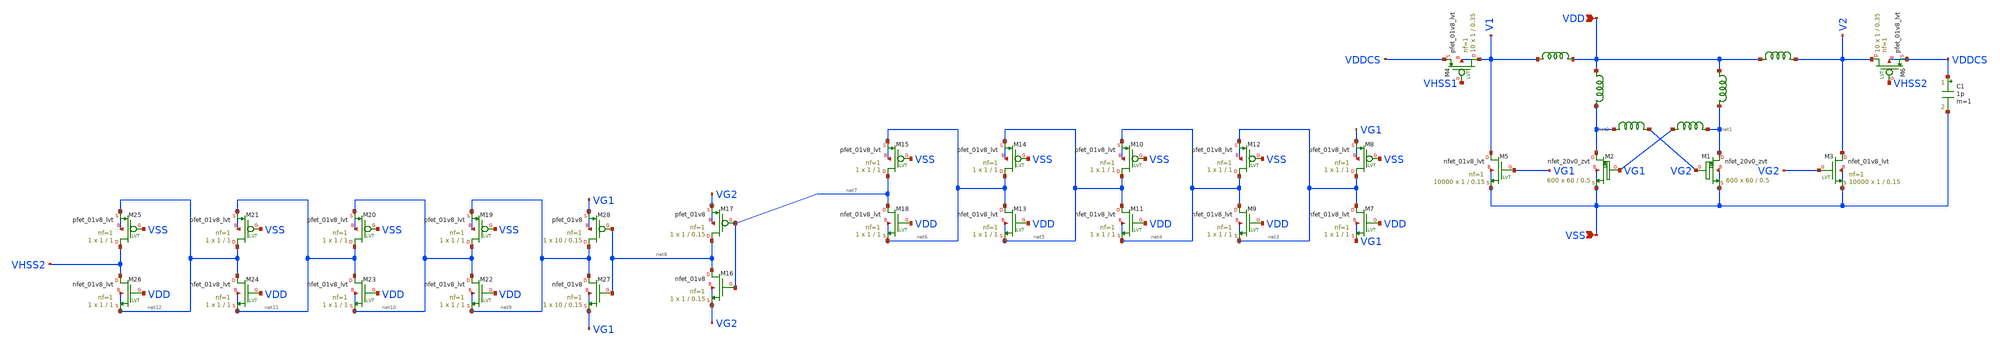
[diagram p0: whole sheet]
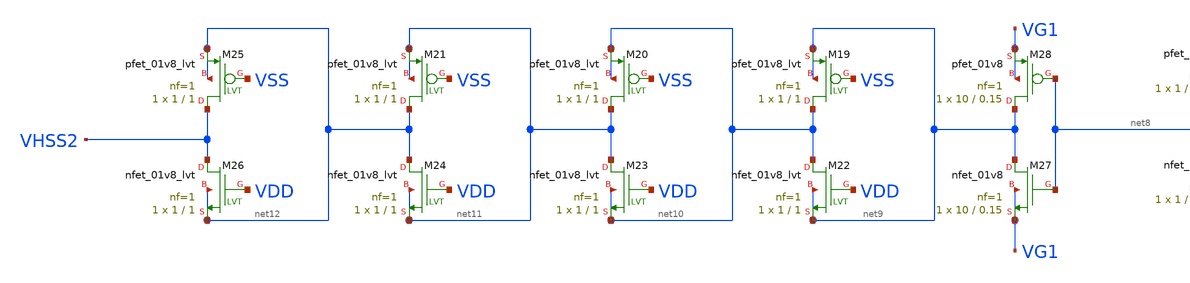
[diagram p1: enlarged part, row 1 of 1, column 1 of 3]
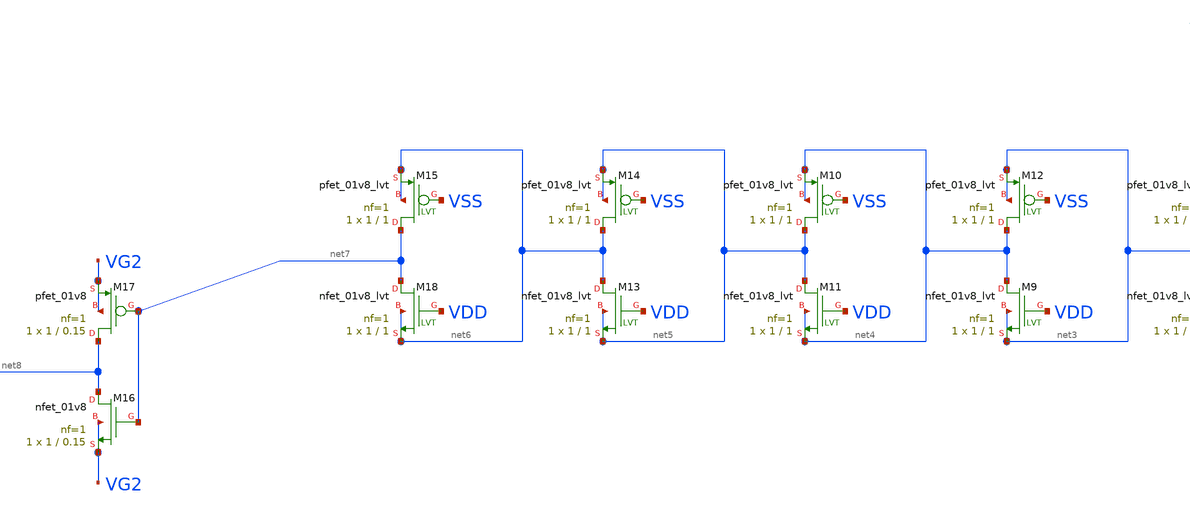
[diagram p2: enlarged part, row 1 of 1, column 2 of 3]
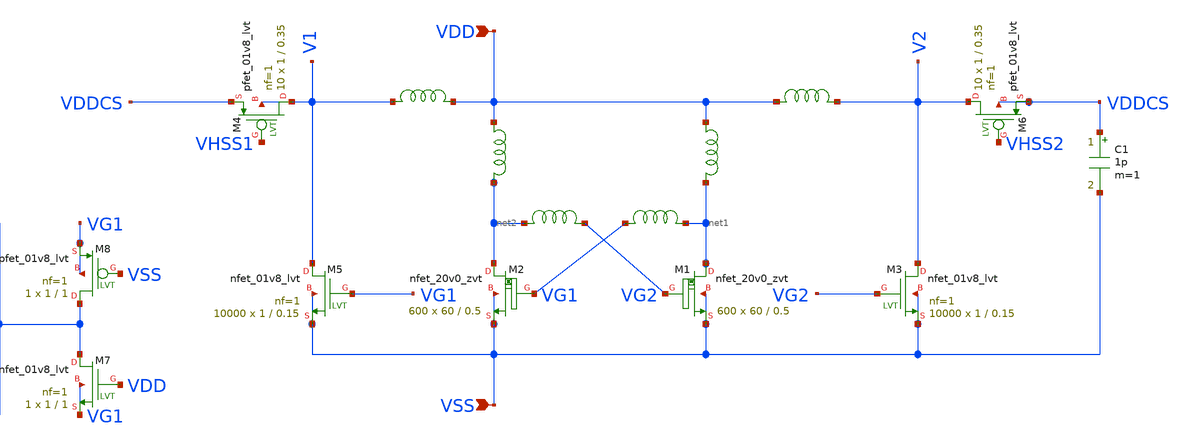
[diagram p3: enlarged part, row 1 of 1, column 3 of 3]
** sch_path: design/LELO_SVOD_SKY130A/LELO_EXSCtwostage.sch
**.subckt LELO_EXSCtwostage VSS VDD
*.ipin VSS
*.ipin VDD
x3 VDD net1 1812PS-102_imp
x4 VDD net2 1812PS-102_imp
XM1 net1 VG2 VSS VSS sky130_fd_pr__nfet_20v0_zvt W=60 L=0.5 m=600
XM2 net2 VG1 VSS VSS sky130_fd_pr__nfet_20v0_zvt W=60 L=0.5 m=600
x1 net2 VG2 1812PS-104_imp
x2 VG1 net1 1812PS-104_imp
C1 VDDCS VSS 1p m=1
x5 VDD V1 1812PS-334_imp
x6 VDD V2 1812PS-334_imp
XM3 V2 VG2 VSS VSS sky130_fd_pr__nfet_01v8_lvt L=0.15 W=1 nf=1 ad='int((1 + 1)/2) * 1 / 1 * 0.29' as='int((1 + 2)/2) * 1 / 1 * 0.29'
+ pd='2*int((1 + 1)/2) * (1 / 1 + 0.29)' ps='2*int((1 + 2)/2) * (1 / 1 + 0.29)' nrd='0.29 / 1 ' nrs='0.29 / 1 '
+ sa=0 sb=0 sd=0 mult=10000 m=10000
XM5 V1 VG1 VSS VSS sky130_fd_pr__nfet_01v8_lvt L=0.15 W=1 nf=1 ad='int((1 + 1)/2) * 1 / 1 * 0.29' as='int((1 + 2)/2) * 1 / 1 * 0.29'
+ pd='2*int((1 + 1)/2) * (1 / 1 + 0.29)' ps='2*int((1 + 2)/2) * (1 / 1 + 0.29)' nrd='0.29 / 1 ' nrs='0.29 / 1 '
+ sa=0 sb=0 sd=0 mult=10000 m=10000
XM6 V2 VHSS2 VDDCS VDDCS sky130_fd_pr__pfet_01v8_lvt L=0.35 W=1 nf=1 ad='int((1 + 1)/2) * 1 / 1 * 0.29'
+ as='int((1 + 2)/2) * 1 / 1 * 0.29' pd='2*int((1 + 1)/2) * (1 / 1 + 0.29)' ps='2*int((1 + 2)/2) * (1 / 1 + 0.29)'
+ nrd='0.29 / 1 ' nrs='0.29 / 1 ' sa=0 sb=0 sd=0 mult=10 m=10
XM4 V1 VHSS1 VDDCS V1 sky130_fd_pr__pfet_01v8_lvt L=0.35 W=1 nf=1 ad='int((1 + 1)/2) * 1 / 1 * 0.29'
+ as='int((1 + 2)/2) * 1 / 1 * 0.29' pd='2*int((1 + 1)/2) * (1 / 1 + 0.29)' ps='2*int((1 + 2)/2) * (1 / 1 + 0.29)'
+ nrd='0.29 / 1 ' nrs='0.29 / 1 ' sa=0 sb=0 sd=0 mult=10 m=10
XM8 net3 VSS VG1 VG1 sky130_fd_pr__pfet_01v8_lvt L=1 W=1 nf=1 ad='int((1 + 1)/2) * 1 / 1 * 0.29' as='int((1 + 2)/2) * 1 / 1 * 0.29'
+ pd='2*int((1 + 1)/2) * (1 / 1 + 0.29)' ps='2*int((1 + 2)/2) * (1 / 1 + 0.29)' nrd='0.29 / 1 ' nrs='0.29 / 1 '
+ sa=0 sb=0 sd=0 mult=1 m=1
XM12 net4 VSS net3 net3 sky130_fd_pr__pfet_01v8_lvt L=1 W=1 nf=1 ad='int((1 + 1)/2) * 1 / 1 * 0.29' as='int((1 + 2)/2) * 1 / 1 * 0.29'
+ pd='2*int((1 + 1)/2) * (1 / 1 + 0.29)' ps='2*int((1 + 2)/2) * (1 / 1 + 0.29)' nrd='0.29 / 1 ' nrs='0.29 / 1 '
+ sa=0 sb=0 sd=0 mult=1 m=1
XM10 net5 VSS net4 net4 sky130_fd_pr__pfet_01v8_lvt L=1 W=1 nf=1 ad='int((1 + 1)/2) * 1 / 1 * 0.29' as='int((1 + 2)/2) * 1 / 1 * 0.29'
+ pd='2*int((1 + 1)/2) * (1 / 1 + 0.29)' ps='2*int((1 + 2)/2) * (1 / 1 + 0.29)' nrd='0.29 / 1 ' nrs='0.29 / 1 '
+ sa=0 sb=0 sd=0 mult=1 m=1
XM14 net6 VSS net5 net5 sky130_fd_pr__pfet_01v8_lvt L=1 W=1 nf=1 ad='int((1 + 1)/2) * 1 / 1 * 0.29' as='int((1 + 2)/2) * 1 / 1 * 0.29'
+ pd='2*int((1 + 1)/2) * (1 / 1 + 0.29)' ps='2*int((1 + 2)/2) * (1 / 1 + 0.29)' nrd='0.29 / 1 ' nrs='0.29 / 1 '
+ sa=0 sb=0 sd=0 mult=1 m=1
XM7 net3 VDD VG1 VG1 sky130_fd_pr__nfet_01v8_lvt L=1 W=1 nf=1 ad='int((1 + 1)/2) * 1 / 1 * 0.29' as='int((1 + 2)/2) * 1 / 1 * 0.29'
+ pd='2*int((1 + 1)/2) * (1 / 1 + 0.29)' ps='2*int((1 + 2)/2) * (1 / 1 + 0.29)' nrd='0.29 / 1 ' nrs='0.29 / 1 '
+ sa=0 sb=0 sd=0 mult=1 m=1
XM9 net4 VDD net3 net3 sky130_fd_pr__nfet_01v8_lvt L=1 W=1 nf=1 ad='int((1 + 1)/2) * 1 / 1 * 0.29' as='int((1 + 2)/2) * 1 / 1 * 0.29'
+ pd='2*int((1 + 1)/2) * (1 / 1 + 0.29)' ps='2*int((1 + 2)/2) * (1 / 1 + 0.29)' nrd='0.29 / 1 ' nrs='0.29 / 1 '
+ sa=0 sb=0 sd=0 mult=1 m=1
XM11 net5 VDD net4 net4 sky130_fd_pr__nfet_01v8_lvt L=1 W=1 nf=1 ad='int((1 + 1)/2) * 1 / 1 * 0.29' as='int((1 + 2)/2) * 1 / 1 * 0.29'
+ pd='2*int((1 + 1)/2) * (1 / 1 + 0.29)' ps='2*int((1 + 2)/2) * (1 / 1 + 0.29)' nrd='0.29 / 1 ' nrs='0.29 / 1 '
+ sa=0 sb=0 sd=0 mult=1 m=1
XM13 net6 VDD net5 net5 sky130_fd_pr__nfet_01v8_lvt L=1 W=1 nf=1 ad='int((1 + 1)/2) * 1 / 1 * 0.29' as='int((1 + 2)/2) * 1 / 1 * 0.29'
+ pd='2*int((1 + 1)/2) * (1 / 1 + 0.29)' ps='2*int((1 + 2)/2) * (1 / 1 + 0.29)' nrd='0.29 / 1 ' nrs='0.29 / 1 '
+ sa=0 sb=0 sd=0 mult=1 m=1
XM15 net7 VSS net6 net6 sky130_fd_pr__pfet_01v8_lvt L=1 W=1 nf=1 ad='int((1 + 1)/2) * 1 / 1 * 0.29' as='int((1 + 2)/2) * 1 / 1 * 0.29'
+ pd='2*int((1 + 1)/2) * (1 / 1 + 0.29)' ps='2*int((1 + 2)/2) * (1 / 1 + 0.29)' nrd='0.29 / 1 ' nrs='0.29 / 1 '
+ sa=0 sb=0 sd=0 mult=1 m=1
XM18 net7 VDD net6 net6 sky130_fd_pr__nfet_01v8_lvt L=1 W=1 nf=1 ad='int((1 + 1)/2) * 1 / 1 * 0.29' as='int((1 + 2)/2) * 1 / 1 * 0.29'
+ pd='2*int((1 + 1)/2) * (1 / 1 + 0.29)' ps='2*int((1 + 2)/2) * (1 / 1 + 0.29)' nrd='0.29 / 1 ' nrs='0.29 / 1 '
+ sa=0 sb=0 sd=0 mult=1 m=1
XM16 net8 net7 VG2 VG2 sky130_fd_pr__nfet_01v8 L=0.15 W=1 nf=1 ad='int((1 + 1)/2) * 1 / 1 * 0.29' as='int((1 + 2)/2) * 1 / 1 * 0.29'
+ pd='2*int((1 + 1)/2) * (1 / 1 + 0.29)' ps='2*int((1 + 2)/2) * (1 / 1 + 0.29)' nrd='0.29 / 1 ' nrs='0.29 / 1 '
+ sa=0 sb=0 sd=0 mult=1 m=1
XM17 net8 net7 VG2 VG2 sky130_fd_pr__pfet_01v8 L=0.15 W=1 nf=1 ad='int((1 + 1)/2) * 1 / 1 * 0.29' as='int((1 + 2)/2) * 1 / 1 * 0.29'
+ pd='2*int((1 + 1)/2) * (1 / 1 + 0.29)' ps='2*int((1 + 2)/2) * (1 / 1 + 0.29)' nrd='0.29 / 1 ' nrs='0.29 / 1 '
+ sa=0 sb=0 sd=0 mult=1 m=1
XM27 net9 net8 VG1 VG1 sky130_fd_pr__nfet_01v8 L=0.15 W=10 nf=1 ad='int((1 + 1)/2) * 10 / 1 * 0.29' as='int((1 + 2)/2) * 10 / 1 * 0.29'
+ pd='2*int((1 + 1)/2) * (10 / 1 + 0.29)' ps='2*int((1 + 2)/2) * (10 / 1 + 0.29)' nrd='0.29 / 10 ' nrs='0.29 / 10 '
+ sa=0 sb=0 sd=0 mult=1 m=1
XM28 net9 net8 VG1 VG1 sky130_fd_pr__pfet_01v8 L=0.15 W=10 nf=1 ad='int((1 + 1)/2) * 10 / 1 * 0.29' as='int((1 + 2)/2) * 10 / 1 * 0.29'
+ pd='2*int((1 + 1)/2) * (10 / 1 + 0.29)' ps='2*int((1 + 2)/2) * (10 / 1 + 0.29)' nrd='0.29 / 10 ' nrs='0.29 / 10 '
+ sa=0 sb=0 sd=0 mult=1 m=1
XM19 net10 VSS net9 net9 sky130_fd_pr__pfet_01v8_lvt L=1 W=1 nf=1 ad='int((1 + 1)/2) * 1 / 1 * 0.29'
+ as='int((1 + 2)/2) * 1 / 1 * 0.29' pd='2*int((1 + 1)/2) * (1 / 1 + 0.29)' ps='2*int((1 + 2)/2) * (1 / 1 + 0.29)'
+ nrd='0.29 / 1 ' nrs='0.29 / 1 ' sa=0 sb=0 sd=0 mult=1 m=1
XM20 net11 VSS net10 net10 sky130_fd_pr__pfet_01v8_lvt L=1 W=1 nf=1 ad='int((1 + 1)/2) * 1 / 1 * 0.29'
+ as='int((1 + 2)/2) * 1 / 1 * 0.29' pd='2*int((1 + 1)/2) * (1 / 1 + 0.29)' ps='2*int((1 + 2)/2) * (1 / 1 + 0.29)'
+ nrd='0.29 / 1 ' nrs='0.29 / 1 ' sa=0 sb=0 sd=0 mult=1 m=1
XM21 net12 VSS net11 net11 sky130_fd_pr__pfet_01v8_lvt L=1 W=1 nf=1 ad='int((1 + 1)/2) * 1 / 1 * 0.29'
+ as='int((1 + 2)/2) * 1 / 1 * 0.29' pd='2*int((1 + 1)/2) * (1 / 1 + 0.29)' ps='2*int((1 + 2)/2) * (1 / 1 + 0.29)'
+ nrd='0.29 / 1 ' nrs='0.29 / 1 ' sa=0 sb=0 sd=0 mult=1 m=1
XM22 net10 VDD net9 net9 sky130_fd_pr__nfet_01v8_lvt L=1 W=1 nf=1 ad='int((1 + 1)/2) * 1 / 1 * 0.29'
+ as='int((1 + 2)/2) * 1 / 1 * 0.29' pd='2*int((1 + 1)/2) * (1 / 1 + 0.29)' ps='2*int((1 + 2)/2) * (1 / 1 + 0.29)'
+ nrd='0.29 / 1 ' nrs='0.29 / 1 ' sa=0 sb=0 sd=0 mult=1 m=1
XM23 net11 VDD net10 net10 sky130_fd_pr__nfet_01v8_lvt L=1 W=1 nf=1 ad='int((1 + 1)/2) * 1 / 1 * 0.29'
+ as='int((1 + 2)/2) * 1 / 1 * 0.29' pd='2*int((1 + 1)/2) * (1 / 1 + 0.29)' ps='2*int((1 + 2)/2) * (1 / 1 + 0.29)'
+ nrd='0.29 / 1 ' nrs='0.29 / 1 ' sa=0 sb=0 sd=0 mult=1 m=1
XM24 net12 VDD net11 net11 sky130_fd_pr__nfet_01v8_lvt L=1 W=1 nf=1 ad='int((1 + 1)/2) * 1 / 1 * 0.29'
+ as='int((1 + 2)/2) * 1 / 1 * 0.29' pd='2*int((1 + 1)/2) * (1 / 1 + 0.29)' ps='2*int((1 + 2)/2) * (1 / 1 + 0.29)'
+ nrd='0.29 / 1 ' nrs='0.29 / 1 ' sa=0 sb=0 sd=0 mult=1 m=1
XM25 VHSS2 VSS net12 net12 sky130_fd_pr__pfet_01v8_lvt L=1 W=1 nf=1 ad='int((1 + 1)/2) * 1 / 1 * 0.29'
+ as='int((1 + 2)/2) * 1 / 1 * 0.29' pd='2*int((1 + 1)/2) * (1 / 1 + 0.29)' ps='2*int((1 + 2)/2) * (1 / 1 + 0.29)'
+ nrd='0.29 / 1 ' nrs='0.29 / 1 ' sa=0 sb=0 sd=0 mult=1 m=1
XM26 VHSS2 VDD net12 net12 sky130_fd_pr__nfet_01v8_lvt L=1 W=1 nf=1 ad='int((1 + 1)/2) * 1 / 1 * 0.29'
+ as='int((1 + 2)/2) * 1 / 1 * 0.29' pd='2*int((1 + 1)/2) * (1 / 1 + 0.29)' ps='2*int((1 + 2)/2) * (1 / 1 + 0.29)'
+ nrd='0.29 / 1 ' nrs='0.29 / 1 ' sa=0 sb=0 sd=0 mult=1 m=1
**.ends

* expanding   symbol:  LELO_SVOD_SKY130A/1812PS-102_imp.sym # of pins=2
** sym_path: design/LELO_SVOD_SKY130A/1812PS-102_imp.sym

.subckt 1812PS-102_imp port1 port2
X1 port1 port2 Model1D R1=60 R2=0.054 C= 0.15p K1=0.000001 K2=0.064 K3= 1u K4=1E-06 K5=0.000001 L=0
+ Is=0 a=0 L_Z0=0 L_EL=0 L_F0=0E6 PkZ=1282.46492
.ends 1812PS-102_imp

* expanding   symbol:  LELO_SVOD_SKY130A/1812PS-104_imp.sym # of pins=2
** sym_path: design/LELO_SVOD_SKY130A/1812PS-104_imp.sym

.subckt 1812PS-104_imp port1 port2
X1 port1 port2 Model1D R1=40 R2=1.3 C= 1.6p K1=0.000001 K2=13.98 K3= 100u K4=0.000001 K5=0.000001
+ L=0 Is=0 a=0 L_Z0=0 L_EL=0 L_F0=0E6 PkZ=48065.0165
.ends 1812PS-104_imp

* expanding   symbol:  LELO_SVOD_SKY130A/1812PS-334_imp.sym # of pins=2
** sym_path: design/LELO_SVOD_SKY130A/1812PS-334_imp.sym

.subckt 1812PS-334_imp port1 port2
X1 port1 port2 Model1D R1=75 R2=4.9 C= 2.43p K1=1E-06 K2=57.9 K3= 330u K4=0.000001 K5=0.000001 L=0
+ Is=0 a=0 L_Z0=0 L_EL=0 L_F0=0E6 PkZ=127597.141
.ends 1812PS-334_imp

.end
